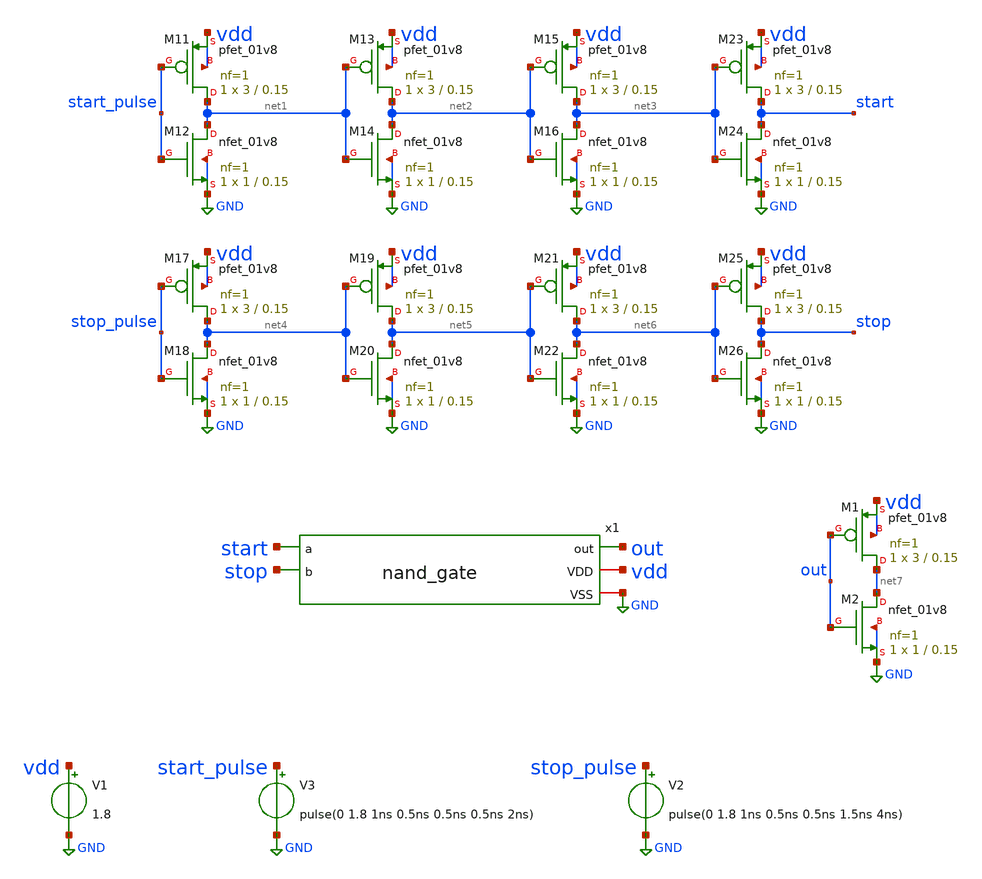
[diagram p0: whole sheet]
** sch_path: xschem/nand_gate_tb.sch
**.subckt nand_gate_tb
x1 start stop out vdd GND nand_gate
V2 stop_pulse GND pulse(0 1.8 1ns 0.5ns 0.5ns 1.5ns 4ns)
V3 start_pulse GND pulse(0 1.8 1ns 0.5ns 0.5ns 0.5ns 2ns)
XM11 net1 start_pulse vdd vdd sky130_fd_pr__pfet_01v8 L=0.15 W=3 nf=1 ad='int((nf+1)/2) * W/nf * 0.29'
+ as='int((nf+2)/2) * W/nf * 0.29' pd='2*int((nf+1)/2) * (W/nf + 0.29)' ps='2*int((nf+2)/2) * (W/nf + 0.29)'
+ nrd='0.29 / W' nrs='0.29 / W' sa=0 sb=0 sd=0 mult=1 m=1
XM12 net1 start_pulse GND GND sky130_fd_pr__nfet_01v8 L=0.15 W=1 nf=1 ad='int((nf+1)/2) * W/nf * 0.29'
+ as='int((nf+2)/2) * W/nf * 0.29' pd='2*int((nf+1)/2) * (W/nf + 0.29)' ps='2*int((nf+2)/2) * (W/nf + 0.29)'
+ nrd='0.29 / W' nrs='0.29 / W' sa=0 sb=0 sd=0 mult=1 m=1
XM13 net2 net1 vdd vdd sky130_fd_pr__pfet_01v8 L=0.15 W=3 nf=1 ad='int((nf+1)/2) * W/nf * 0.29' as='int((nf+2)/2) * W/nf * 0.29'
+ pd='2*int((nf+1)/2) * (W/nf + 0.29)' ps='2*int((nf+2)/2) * (W/nf + 0.29)' nrd='0.29 / W' nrs='0.29 / W'
+ sa=0 sb=0 sd=0 mult=1 m=1
XM14 net2 net1 GND GND sky130_fd_pr__nfet_01v8 L=0.15 W=1 nf=1 ad='int((nf+1)/2) * W/nf * 0.29' as='int((nf+2)/2) * W/nf * 0.29'
+ pd='2*int((nf+1)/2) * (W/nf + 0.29)' ps='2*int((nf+2)/2) * (W/nf + 0.29)' nrd='0.29 / W' nrs='0.29 / W'
+ sa=0 sb=0 sd=0 mult=1 m=1
XM15 net3 net2 vdd vdd sky130_fd_pr__pfet_01v8 L=0.15 W=3 nf=1 ad='int((nf+1)/2) * W/nf * 0.29' as='int((nf+2)/2) * W/nf * 0.29'
+ pd='2*int((nf+1)/2) * (W/nf + 0.29)' ps='2*int((nf+2)/2) * (W/nf + 0.29)' nrd='0.29 / W' nrs='0.29 / W'
+ sa=0 sb=0 sd=0 mult=1 m=1
XM16 net3 net2 GND GND sky130_fd_pr__nfet_01v8 L=0.15 W=1 nf=1 ad='int((nf+1)/2) * W/nf * 0.29' as='int((nf+2)/2) * W/nf * 0.29'
+ pd='2*int((nf+1)/2) * (W/nf + 0.29)' ps='2*int((nf+2)/2) * (W/nf + 0.29)' nrd='0.29 / W' nrs='0.29 / W'
+ sa=0 sb=0 sd=0 mult=1 m=1
XM17 net4 stop_pulse vdd vdd sky130_fd_pr__pfet_01v8 L=0.15 W=3 nf=1 ad='int((nf+1)/2) * W/nf * 0.29'
+ as='int((nf+2)/2) * W/nf * 0.29' pd='2*int((nf+1)/2) * (W/nf + 0.29)' ps='2*int((nf+2)/2) * (W/nf + 0.29)'
+ nrd='0.29 / W' nrs='0.29 / W' sa=0 sb=0 sd=0 mult=1 m=1
XM18 net4 stop_pulse GND GND sky130_fd_pr__nfet_01v8 L=0.15 W=1 nf=1 ad='int((nf+1)/2) * W/nf * 0.29'
+ as='int((nf+2)/2) * W/nf * 0.29' pd='2*int((nf+1)/2) * (W/nf + 0.29)' ps='2*int((nf+2)/2) * (W/nf + 0.29)'
+ nrd='0.29 / W' nrs='0.29 / W' sa=0 sb=0 sd=0 mult=1 m=1
XM19 net5 net4 vdd vdd sky130_fd_pr__pfet_01v8 L=0.15 W=3 nf=1 ad='int((nf+1)/2) * W/nf * 0.29' as='int((nf+2)/2) * W/nf * 0.29'
+ pd='2*int((nf+1)/2) * (W/nf + 0.29)' ps='2*int((nf+2)/2) * (W/nf + 0.29)' nrd='0.29 / W' nrs='0.29 / W'
+ sa=0 sb=0 sd=0 mult=1 m=1
XM20 net5 net4 GND GND sky130_fd_pr__nfet_01v8 L=0.15 W=1 nf=1 ad='int((nf+1)/2) * W/nf * 0.29' as='int((nf+2)/2) * W/nf * 0.29'
+ pd='2*int((nf+1)/2) * (W/nf + 0.29)' ps='2*int((nf+2)/2) * (W/nf + 0.29)' nrd='0.29 / W' nrs='0.29 / W'
+ sa=0 sb=0 sd=0 mult=1 m=1
XM21 net6 net5 vdd vdd sky130_fd_pr__pfet_01v8 L=0.15 W=3 nf=1 ad='int((nf+1)/2) * W/nf * 0.29' as='int((nf+2)/2) * W/nf * 0.29'
+ pd='2*int((nf+1)/2) * (W/nf + 0.29)' ps='2*int((nf+2)/2) * (W/nf + 0.29)' nrd='0.29 / W' nrs='0.29 / W'
+ sa=0 sb=0 sd=0 mult=1 m=1
XM22 net6 net5 GND GND sky130_fd_pr__nfet_01v8 L=0.15 W=1 nf=1 ad='int((nf+1)/2) * W/nf * 0.29' as='int((nf+2)/2) * W/nf * 0.29'
+ pd='2*int((nf+1)/2) * (W/nf + 0.29)' ps='2*int((nf+2)/2) * (W/nf + 0.29)' nrd='0.29 / W' nrs='0.29 / W'
+ sa=0 sb=0 sd=0 mult=1 m=1
XM23 start net3 vdd vdd sky130_fd_pr__pfet_01v8 L=0.15 W=3 nf=1 ad='int((nf+1)/2) * W/nf * 0.29' as='int((nf+2)/2) * W/nf * 0.29'
+ pd='2*int((nf+1)/2) * (W/nf + 0.29)' ps='2*int((nf+2)/2) * (W/nf + 0.29)' nrd='0.29 / W' nrs='0.29 / W'
+ sa=0 sb=0 sd=0 mult=1 m=1
XM24 start net3 GND GND sky130_fd_pr__nfet_01v8 L=0.15 W=1 nf=1 ad='int((nf+1)/2) * W/nf * 0.29' as='int((nf+2)/2) * W/nf * 0.29'
+ pd='2*int((nf+1)/2) * (W/nf + 0.29)' ps='2*int((nf+2)/2) * (W/nf + 0.29)' nrd='0.29 / W' nrs='0.29 / W'
+ sa=0 sb=0 sd=0 mult=1 m=1
XM25 stop net6 vdd vdd sky130_fd_pr__pfet_01v8 L=0.15 W=3 nf=1 ad='int((nf+1)/2) * W/nf * 0.29' as='int((nf+2)/2) * W/nf * 0.29'
+ pd='2*int((nf+1)/2) * (W/nf + 0.29)' ps='2*int((nf+2)/2) * (W/nf + 0.29)' nrd='0.29 / W' nrs='0.29 / W'
+ sa=0 sb=0 sd=0 mult=1 m=1
XM26 stop net6 GND GND sky130_fd_pr__nfet_01v8 L=0.15 W=1 nf=1 ad='int((nf+1)/2) * W/nf * 0.29' as='int((nf+2)/2) * W/nf * 0.29'
+ pd='2*int((nf+1)/2) * (W/nf + 0.29)' ps='2*int((nf+2)/2) * (W/nf + 0.29)' nrd='0.29 / W' nrs='0.29 / W'
+ sa=0 sb=0 sd=0 mult=1 m=1
XM1 net7 out vdd vdd sky130_fd_pr__pfet_01v8 L=0.15 W=3 nf=1 ad='int((nf+1)/2) * W/nf * 0.29' as='int((nf+2)/2) * W/nf * 0.29'
+ pd='2*int((nf+1)/2) * (W/nf + 0.29)' ps='2*int((nf+2)/2) * (W/nf + 0.29)' nrd='0.29 / W' nrs='0.29 / W'
+ sa=0 sb=0 sd=0 mult=1 m=1
XM2 net7 out GND GND sky130_fd_pr__nfet_01v8 L=0.15 W=1 nf=1 ad='int((nf+1)/2) * W/nf * 0.29' as='int((nf+2)/2) * W/nf * 0.29'
+ pd='2*int((nf+1)/2) * (W/nf + 0.29)' ps='2*int((nf+2)/2) * (W/nf + 0.29)' nrd='0.29 / W' nrs='0.29 / W'
+ sa=0 sb=0 sd=0 mult=1 m=1
V1 vdd GND 1.8
**** begin user architecture code

** opencircuitdesign pdks install
.lib $::SKYWATER_MODELS/sky130.lib.spice tt





.tran 0.001n 5n
.save v(start) v(stop) v(out)

.control
run
set wr_vecnames
wrdata nand_gate_tb.txt v(start) v(stop) v(out)
.endc


**** end user architecture code
**.ends

* expanding   symbol:  nand_gate.sym # of pins=5
** sym_path: xschem/nand_gate.sym
** sch_path: xschem/nand_gate.sch
.subckt nand_gate a b out VDD VSS
*.iopin VDD
*.ipin a
*.opin out
*.iopin VSS
*.ipin b
XM7 out a net1 VSS sky130_fd_pr__nfet_01v8 L=0.15 W=2 nf=1 ad='int((nf+1)/2) * W/nf * 0.29' as='int((nf+2)/2) * W/nf * 0.29'
+ pd='2*int((nf+1)/2) * (W/nf + 0.29)' ps='2*int((nf+2)/2) * (W/nf + 0.29)' nrd='0.29 / W' nrs='0.29 / W'
+ sa=0 sb=0 sd=0 mult=1 m=1
XM1 out a VDD VDD sky130_fd_pr__pfet_01v8 L=0.15 W=3 nf=1 ad='int((nf+1)/2) * W/nf * 0.29' as='int((nf+2)/2) * W/nf * 0.29'
+ pd='2*int((nf+1)/2) * (W/nf + 0.29)' ps='2*int((nf+2)/2) * (W/nf + 0.29)' nrd='0.29 / W' nrs='0.29 / W'
+ sa=0 sb=0 sd=0 mult=1 m=1
XM2 net1 b VSS VSS sky130_fd_pr__nfet_01v8 L=0.15 W=2 nf=1 ad='int((nf+1)/2) * W/nf * 0.29' as='int((nf+2)/2) * W/nf * 0.29'
+ pd='2*int((nf+1)/2) * (W/nf + 0.29)' ps='2*int((nf+2)/2) * (W/nf + 0.29)' nrd='0.29 / W' nrs='0.29 / W'
+ sa=0 sb=0 sd=0 mult=1 m=1
XM3 out b VDD VDD sky130_fd_pr__pfet_01v8 L=0.15 W=3 nf=1 ad='int((nf+1)/2) * W/nf * 0.29' as='int((nf+2)/2) * W/nf * 0.29'
+ pd='2*int((nf+1)/2) * (W/nf + 0.29)' ps='2*int((nf+2)/2) * (W/nf + 0.29)' nrd='0.29 / W' nrs='0.29 / W'
+ sa=0 sb=0 sd=0 mult=1 m=1
.ends

.GLOBAL GND
.end
